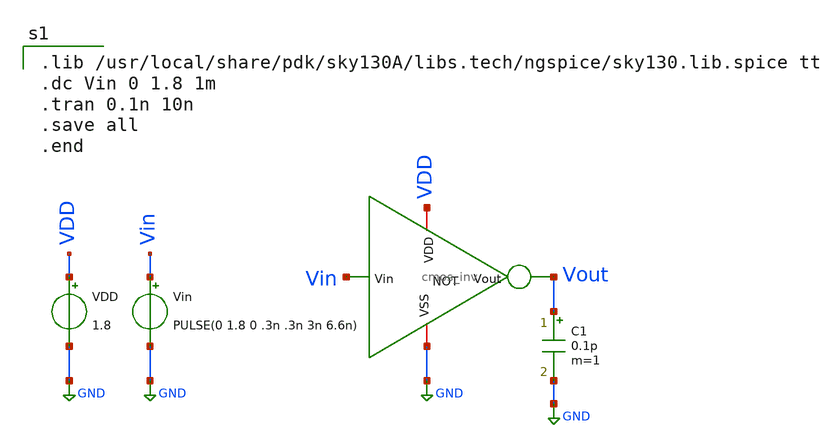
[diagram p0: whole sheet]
** sch_path: OneDrive/Documents/CMOS-Inverter-Design-and-Analysis-using-Sky130pdk-main/xschem/cmos_inv_tb.sch
**.subckt cmos_inv_tb
x1 VDD Vin Vout GND cmos_inv
VDD VDD GND 1.8
Vin Vin GND PULSE(0 1.8 0 .3n .3n 3n 6.6n)
C1 Vout GND 0.1p m=1
**** begin user architecture code

.lib /usr/local/share/pdk/sky130A/libs.tech/ngspice/sky130.lib.spice tt
.dc Vin 0 1.8 1m
.tran 0.1n 10n
.save all
.end

**** end user architecture code
**.ends

* expanding   symbol:  cmos_inv.sym # of pins=4
** sym_path: OneDrive/Documents/CMOS-Inverter-Design-and-Analysis-using-Sky130pdk-main/xschem/cmos_inv.sym
** sch_path: OneDrive/Documents/CMOS-Inverter-Design-and-Analysis-using-Sky130pdk-main/xschem/cmos_inv.sch
.subckt cmos_inv VDD Vin Vout VSS
*.iopin VDD
*.iopin VSS
*.ipin Vin
*.opin Vout
XM1 Vout Vin VSS VSS sky130_fd_pr__nfet_01v8 L=0.15 W=1 nf=1 ad='int((1 + 1)/2) * 1 / 1 * 0.29' as='int((1 + 2)/2) * 1 / 1 * 0.29'
+ pd='2*int((1 + 1)/2) * (1 / 1 + 0.29)' ps='2*int((1 + 2)/2) * (1 / 1 + 0.29)' nrd='0.29 / 1 ' nrs='0.29 / 1 '
+ sa=0 sb=0 sd=0 mult=1 m=1
XM2 Vout Vin VDD VDD sky130_fd_pr__pfet_01v8 L=0.15 W=3.5 nf=1 ad='int((1 + 1)/2) * 3.5 / 1 * 0.29' as='int((1 + 2)/2) * 3.5 / 1 * 0.29'
+ pd='2*int((1 + 1)/2) * (3.5 / 1 + 0.29)' ps='2*int((1 + 2)/2) * (3.5 / 1 + 0.29)' nrd='0.29 / 3.5 ' nrs='0.29 / 3.5 '
+ sa=0 sb=0 sd=0 mult=1 m=1
.ends

.GLOBAL GND
.end
